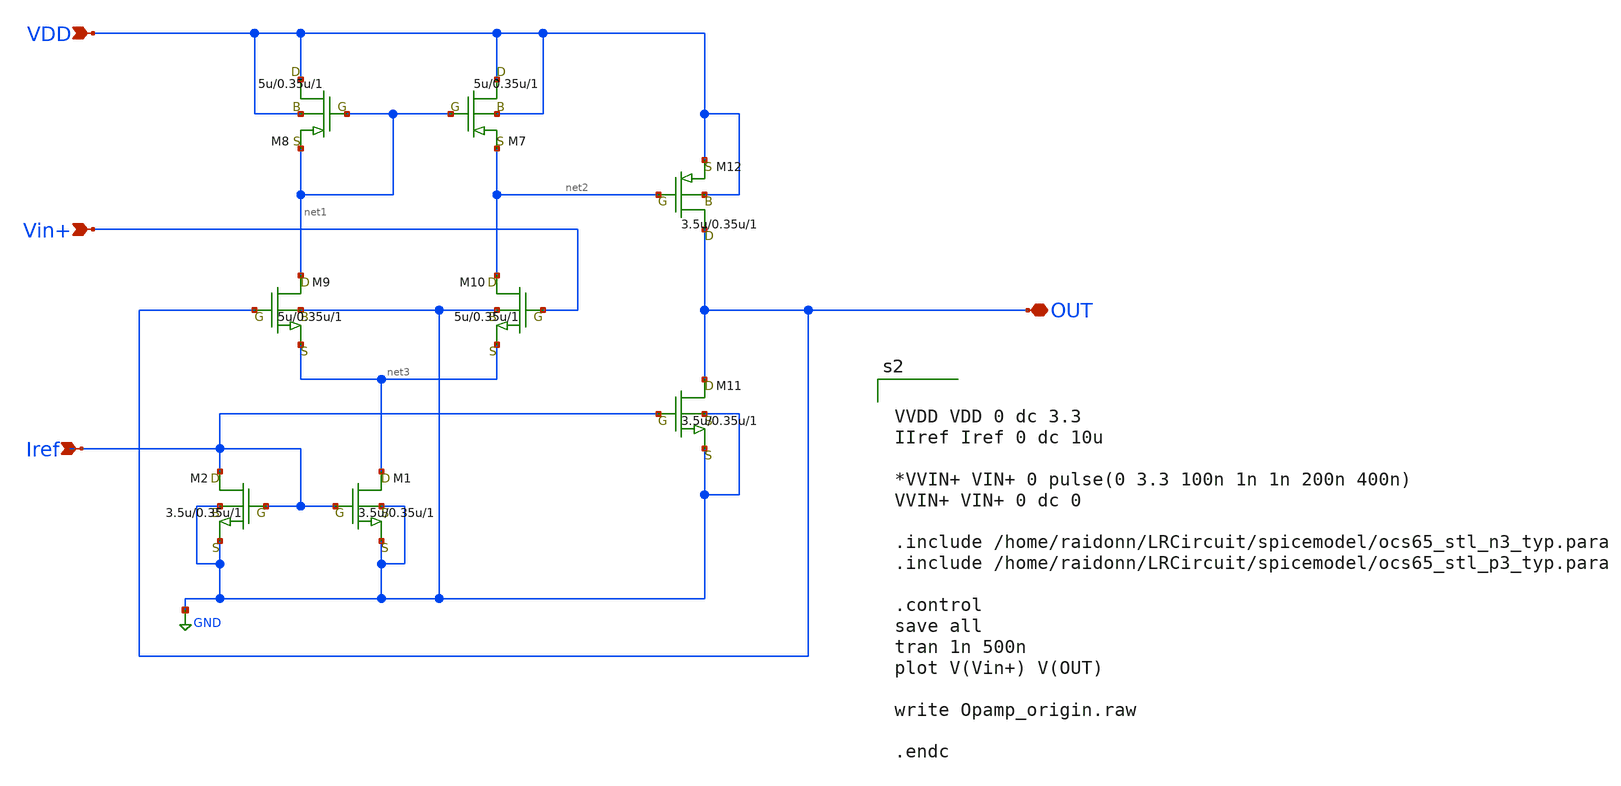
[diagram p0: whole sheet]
** sch_path: LR_Work3/Opamp_before.sch
**.subckt Opamp_before VDD OUT Iref Vin+
*.ipin VDD
*.iopin OUT
*.ipin Iref
*.ipin Vin+
M7 VDD net1 net2 VDD p3.0 w=5u l=0.35u as=0 ps=0 ad=0 pd=0 m=1
M8 VDD net1 net1 VDD p3.0 w=5u l=0.35u as=0 ps=0 ad=0 pd=0 m=1
M9 net1 OUT net3 GND n3.0 w=5u l=0.35u as=0 ps=0 ad=0 pd=0 m=1
M10 net2 Vin+ net3 GND n3.0 w=5u l=0.35u as=0 ps=0 ad=0 pd=0 m=1
M11 OUT Iref GND GND n3.0 w=3.5u l=0.35u as=0 ps=0 ad=0 pd=0 m=1
M12 OUT net2 VDD VDD p3.0 w=3.5u l=0.35u as=0 ps=0 ad=0 pd=0 m=1
M1 net3 Iref GND GND n3.0 w=3.5u l=0.35u as=0 ps=0 ad=0 pd=0 m=1
M2 Iref Iref GND GND n3.0 w=3.5u l=0.35u as=0 ps=0 ad=0 pd=0 m=1
**** begin user architecture code


VVDD VDD 0 dc 3.3
IIref Iref 0 dc 10u

*VVIN+ VIN+ 0 pulse(0 3.3 100n 1n 1n 200n 400n)
VVIN+ VIN+ 0 dc 0

.include /home/raidonn/LRCircuit/spicemodel/ocs65_stl_n3_typ.para
.include /home/raidonn/LRCircuit/spicemodel/ocs65_stl_p3_typ.para

.control
save all
tran 1n 500n
plot V(Vin+) V(OUT)

write Opamp_origin.raw

.endc

**** end user architecture code
**.ends
.GLOBAL GND
.end
